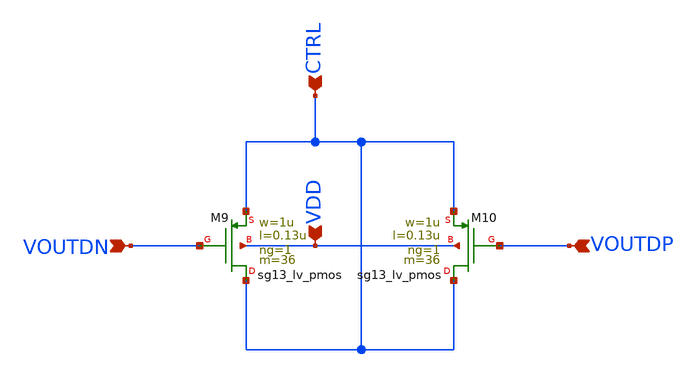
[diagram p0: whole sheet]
** sch_path: 2to4/2to4_decap.sch
**.subckt 2to4_decap CTRL VDD VOUTDN VOUTDP
*.ipin CTRL
*.ipin VDD
*.ipin VOUTDN
*.ipin VOUTDP
XM10 CTRL VOUTDP CTRL VDD sg13_lv_pmos w=1u l=0.13u ng=1 m=36 mm_ok=1
XM9 CTRL VOUTDN CTRL VDD sg13_lv_pmos w=1u l=0.13u ng=1 m=36 mm_ok=1
**.ends
.end
